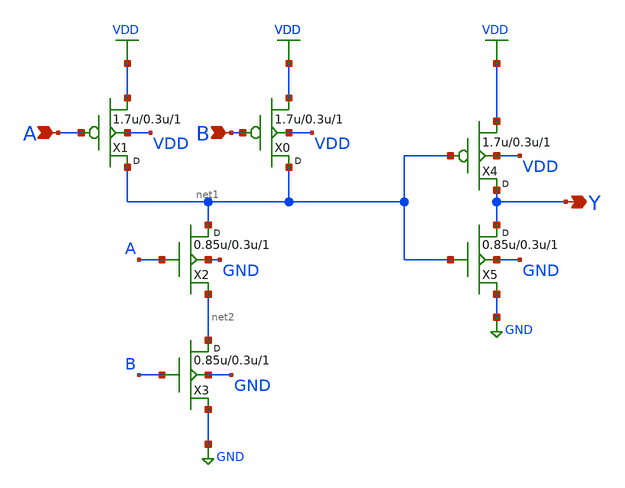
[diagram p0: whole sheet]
** sch_path: lib/xschem/gf180mcu_osu_sc_12T_and2_1.sch
**.subckt gf180mcu_osu_sc_12T_and2_1 A B Y
*.ipin A
*.ipin B
*.opin Y
X1 net1 A VDD VDD pmos_3p3 w=1.7u l=0.3u m=1
X0 net1 B VDD VDD pmos_3p3 w=1.7u l=0.3u m=1
X2 net1 A net2 GND nmos_3p3 w=0.85u l=0.3u m=1
X3 net2 B GND GND nmos_3p3 w=0.85u l=0.3u m=1
X4 Y net1 VDD VDD pmos_3p3 w=1.7u l=0.3u m=1
X5 Y net1 GND GND nmos_3p3 w=0.85u l=0.3u m=1
**** begin user architecture code


.inc "/import/yukari1/lrburle/OSU_180/char/techfiles/design.hspice"
.lib "/import/yukari1/lrburle/OSU_180/char/techfiles/sm141064.hspice" typical


**** end user architecture code
**.ends
.GLOBAL VDD
.GLOBAL GND
.end
